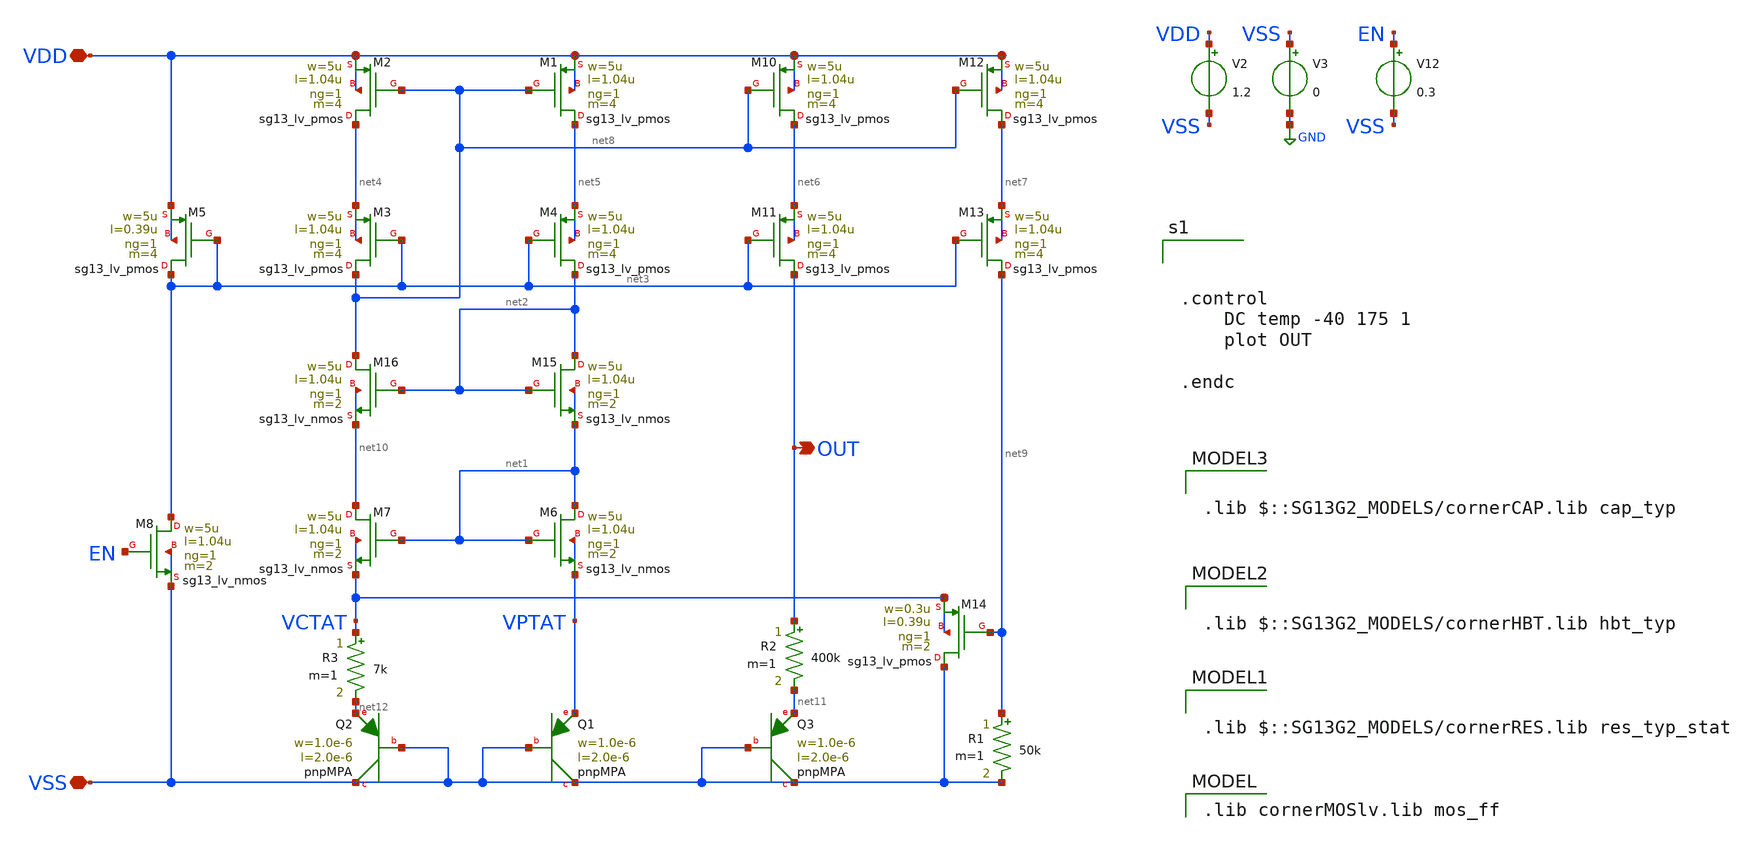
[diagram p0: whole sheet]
** sch_path: libs/core_analog/core_bandgap/testbench/tb_bandgap.sch
**.subckt tb_bandgap VDD VSS OUT
*.iopin VDD
*.iopin VSS
*.opin OUT
V12 EN VSS 0.3
V2 VDD VSS 1.2
V3 VSS GND 0
XM1 net5 net8 VDD VDD sg13_lv_pmos w=5u l=1.04u ng=1 m=4 mm_ok=1
XM2 net4 net8 VDD VDD sg13_lv_pmos w=5u l=1.04u ng=1 m=4 mm_ok=1
XM3 net8 net3 net4 net4 sg13_lv_pmos w=5u l=1.04u ng=1 m=4 mm_ok=1
XM4 net2 net3 net5 net5 sg13_lv_pmos w=5u l=1.04u ng=1 m=4 mm_ok=1
XM5 net3 net3 VDD VDD sg13_lv_pmos w=5u l=0.39u ng=1 m=4 mm_ok=1
XM10 net6 net8 VDD VDD sg13_lv_pmos w=5u l=1.04u ng=1 m=4 mm_ok=1
XM11 OUT net3 net6 net6 sg13_lv_pmos w=5u l=1.04u ng=1 m=4 mm_ok=1
XM12 net7 net8 VDD VDD sg13_lv_pmos w=5u l=1.04u ng=1 m=4 mm_ok=1
XM13 net9 net3 net7 net7 sg13_lv_pmos w=5u l=1.04u ng=1 m=4 mm_ok=1
XQ1 VSS VSS VPTAT pnpMPA a=2p p=6u m=1
XQ2 VSS VSS net12 pnpMPA a=2p p=6u m=8
XQ3 VSS VSS net11 pnpMPA a=2p p=6u m=1
XM14 VSS net9 VCTAT VCTAT sg13_lv_pmos w=0.3u l=0.39u ng=1 m=2 mm_ok=1
XM15 net2 net2 net1 net1 sg13_lv_nmos w=5u l=1.04u ng=1 m=2 mm_ok=1
XM16 net8 net2 net10 net10 sg13_lv_nmos w=5u l=1.04u ng=1 m=2 mm_ok=1
XM6 net1 net1 VPTAT VPTAT sg13_lv_nmos w=5u l=1.04u ng=1 m=2 mm_ok=1
XM7 net10 net1 VCTAT VCTAT sg13_lv_nmos w=5u l=1.04u ng=1 m=2 mm_ok=1
R1 net9 VSS 50k m=1
R2 OUT net11 400k m=1
R3 VCTAT net12 7k m=1
XM8 net3 EN VSS VSS sg13_lv_nmos w=5u l=1.04u ng=1 m=2 mm_ok=1
**** begin user architecture code



.control
	DC temp -40 175 1
	plot OUT

.endc


 .lib cornerMOSlv.lib mos_ff


.lib $::SG13G2_MODELS/cornerRES.lib res_typ_stat


.lib $::SG13G2_MODELS/cornerHBT.lib hbt_typ


.lib $::SG13G2_MODELS/cornerCAP.lib cap_typ

**** end user architecture code
**.ends
.GLOBAL GND
.end
